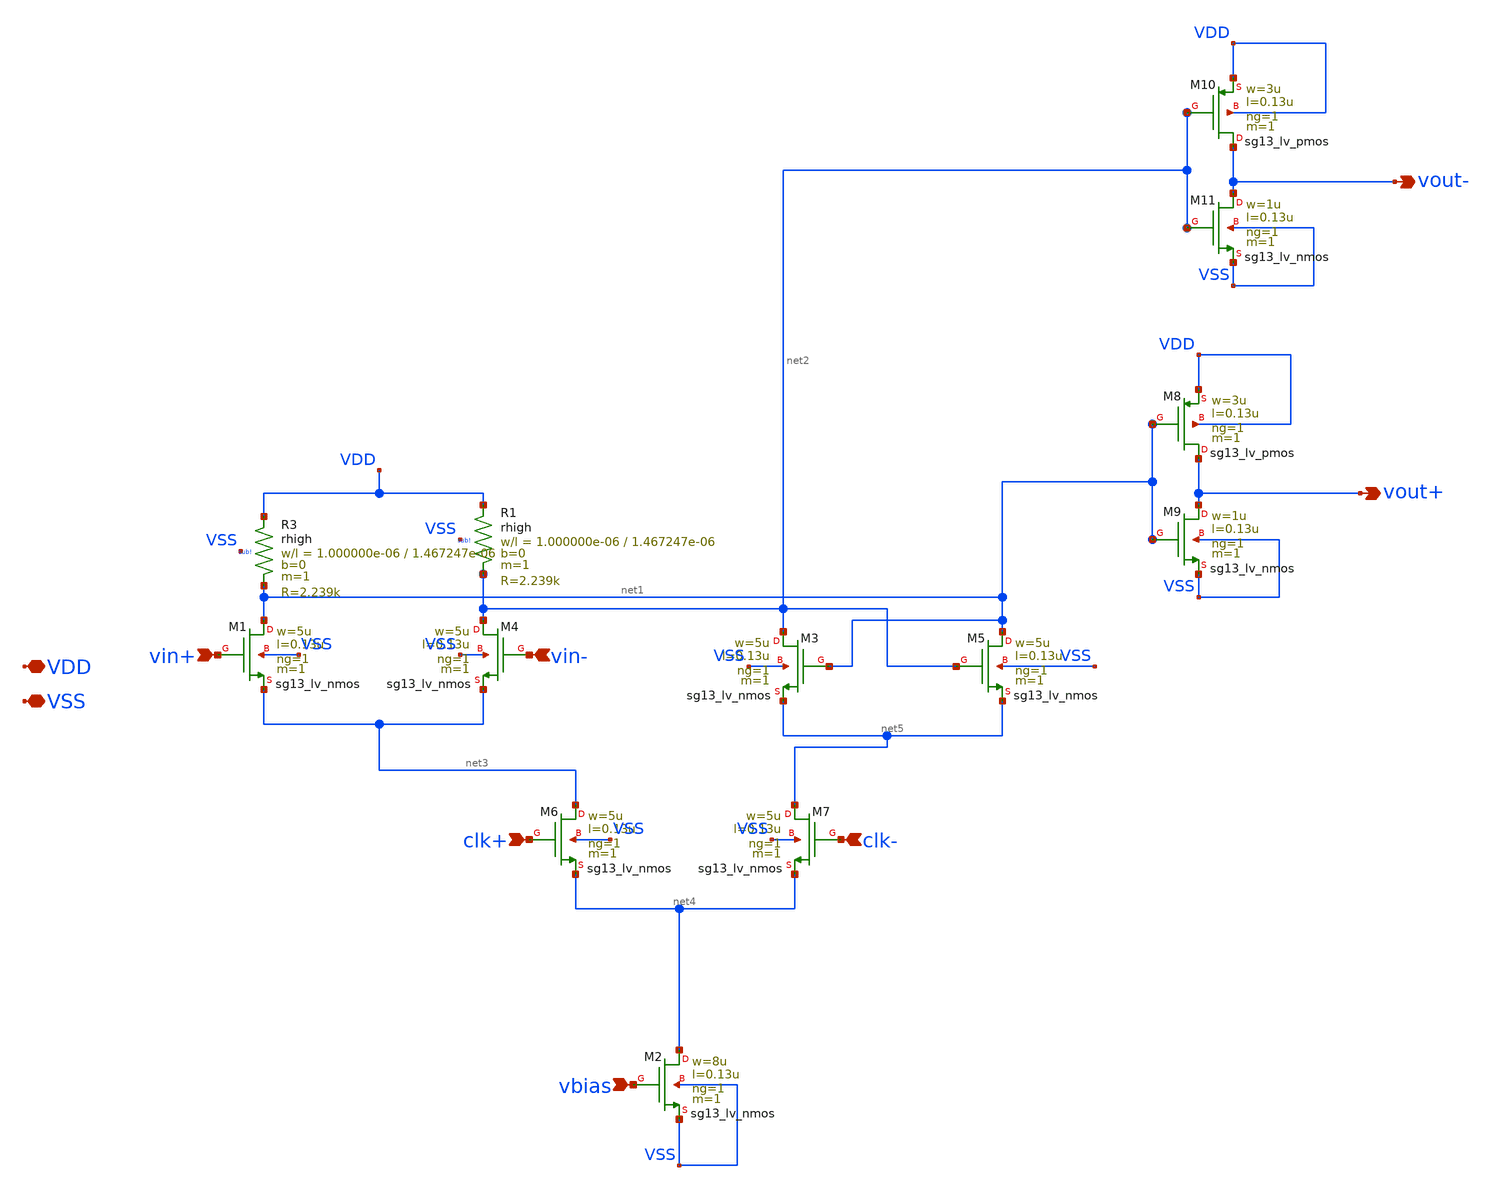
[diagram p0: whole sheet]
** sch_path: xschem/d_latch.sch
**.subckt d_latch VDD VSS vin+ clk- vbias vout+ clk+ vout- vin-
*.iopin VDD
*.iopin VSS
*.ipin vin+
*.ipin clk-
*.ipin vbias
*.opin vout+
*.ipin clk+
*.opin vout-
*.ipin vin-
XM1 net1 vin+ net3 VSS sg13_lv_nmos w=5u l=0.13u ng=1 m=1 mm_ok=1
XM2 net4 vbias VSS VSS sg13_lv_nmos w=8u l=0.13u ng=1 m=1 mm_ok=1
XM4 net2 vin- net3 VSS sg13_lv_nmos w=5u l=0.13u ng=1 m=1 mm_ok=1
XM3 net2 net1 net5 VSS sg13_lv_nmos w=5u l=0.13u ng=1 m=1 mm_ok=1
XM5 net1 net2 net5 VSS sg13_lv_nmos w=5u l=0.13u ng=1 m=1 mm_ok=1
XM6 net3 clk+ net4 VSS sg13_lv_nmos w=5u l=0.13u ng=1 m=1 mm_ok=1
XM7 net5 clk- net4 VSS sg13_lv_nmos w=5u l=0.13u ng=1 m=1 mm_ok=1
XM8 vout+ net1 VDD VDD sg13_lv_pmos w=3u l=0.13u ng=1 m=1 mm_ok=1
XM9 vout+ net1 VSS VSS sg13_lv_nmos w=1u l=0.13u ng=1 m=1 mm_ok=1
XM10 vout- net2 VDD VDD sg13_lv_pmos w=3u l=0.13u ng=1 m=1 mm_ok=1
XM11 vout- net2 VSS VSS sg13_lv_nmos w=1u l=0.13u ng=1 m=1 mm_ok=1
XR3 VDD net1 sub! rhigh w=1.000000e-06 l=1.467247e-06 m=1 b=0 mm_ok=1
XR1 VDD net2 sub! rhigh w=1.000000e-06 l=1.467247e-06 m=1 b=0 mm_ok=1
**.ends
.end
